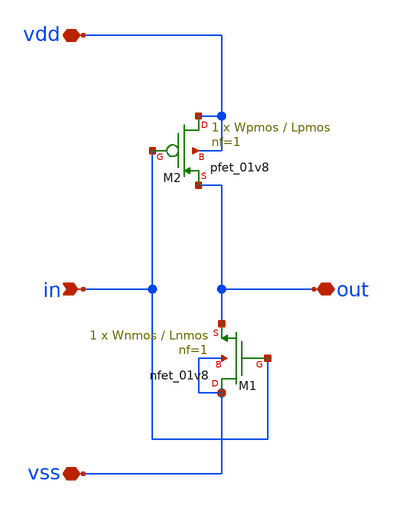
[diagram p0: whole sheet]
** sch_path: xschem/inv/inv.sch
**.subckt inv in out vdd vss
*.ipin in
*.iopin out
*.iopin vdd
*.iopin vss
XM1 vss in out vss sky130_fd_pr__nfet_01v8 L=Lnmos W=Wnmos nf=1 ad='int((nf+1)/2) * W/nf * 0.29' as='int((nf+2)/2) * W/nf * 0.29'
+ pd='2*int((nf+1)/2) * (W/nf + 0.29)' ps='2*int((nf+2)/2) * (W/nf + 0.29)' nrd='0.29 / W' nrs='0.29 / W'
+ sa=0 sb=0 sd=0 mult=1 m=1
XM2 vdd in out vdd sky130_fd_pr__pfet_01v8 L=Lpmos W=Wpmos nf=1 ad='int((nf+1)/2) * W/nf * 0.29' as='int((nf+2)/2) * W/nf * 0.29'
+ pd='2*int((nf+1)/2) * (W/nf + 0.29)' ps='2*int((nf+2)/2) * (W/nf + 0.29)' nrd='0.29 / W' nrs='0.29 / W'
+ sa=0 sb=0 sd=0 mult=1 m=1
**.ends
.end
